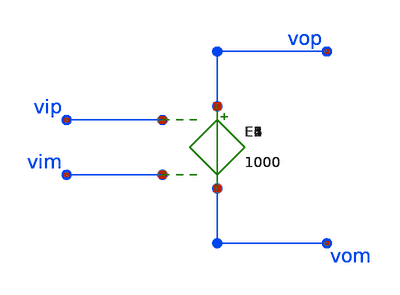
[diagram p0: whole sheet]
** sch_path: xschem/opamp1.sch
**.subckt opamp1
E1 vop vom vip vim 1000
E2 vop vom vip vim 1000
E3 vop vom vip vim 1000
E4 vop vom vip vim 1000
E5 vop vom vip vim 1000
E6 vop vom vip vim 1000
**.ends
.end
